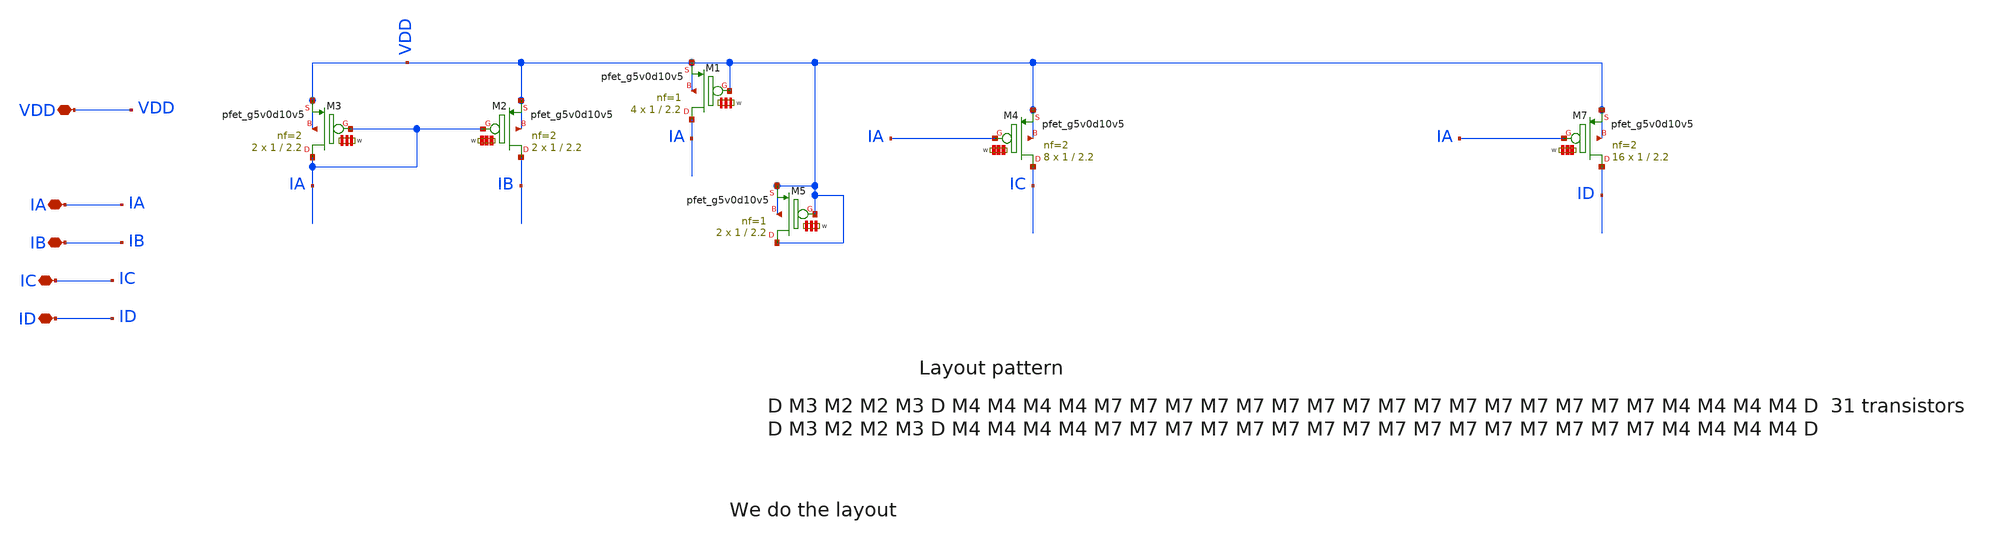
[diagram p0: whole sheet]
** sch_path: Learning/single_ended_amplifiers/Design_and_Analysis_of_Two-Stage_CMOS_Operational_Amplifier_for_Fluorescence_Signal_Processing_sky130_5V/klayout_layout/Pmos_current_mirror.sch
**.subckt Pmos_current_mirror VDD IA IB IC ID
*.iopin VDD
*.iopin IA
*.iopin IB
*.iopin IC
*.iopin ID
XM2 IB IA VDD VDD sky130_fd_pr__pfet_g5v0d10v5 L=2.2 W='1 * 2 ' nf=2 ad='int((2 + 1)/2) * 1 * 0.29' as='int((2 + 2)/2) * 1 * 0.29'
+ pd='2*int((2 + 1)/2) * (1 + 0.29)' ps='2*int((2 + 2)/2) * (1 + 0.29)' nrd='0.29 / 1 / 2 ' nrs='0.29 / 1 / 2 '
+ sa=0 sb=0 sd=0 mult=2 m=2
XM3 IA IA VDD VDD sky130_fd_pr__pfet_g5v0d10v5 L=2.2 W='1 * 2 ' nf=2 ad='int((2 + 1)/2) * 1 * 0.29' as='int((2 + 2)/2) * 1 * 0.29'
+ pd='2*int((2 + 1)/2) * (1 + 0.29)' ps='2*int((2 + 2)/2) * (1 + 0.29)' nrd='0.29 / 1 / 2 ' nrs='0.29 / 1 / 2 '
+ sa=0 sb=0 sd=0 mult=2 m=2
XM4 IC IA VDD VDD sky130_fd_pr__pfet_g5v0d10v5 L=2.2 W='1 * 2 ' nf=2 ad='int((2 + 1)/2) * 1 * 0.29' as='int((2 + 2)/2) * 1 * 0.29'
+ pd='2*int((2 + 1)/2) * (1 + 0.29)' ps='2*int((2 + 2)/2) * (1 + 0.29)' nrd='0.29 / 1 / 2 ' nrs='0.29 / 1 / 2 '
+ sa=0 sb=0 sd=0 mult=8 m=8
XM7 ID IA VDD VDD sky130_fd_pr__pfet_g5v0d10v5 L=2.2 W='1 * 2 ' nf=2 ad='int((2 + 1)/2) * 1 * 0.29' as='int((2 + 2)/2) * 1 * 0.29'
+ pd='2*int((2 + 1)/2) * (1 + 0.29)' ps='2*int((2 + 2)/2) * (1 + 0.29)' nrd='0.29 / 1 / 2 ' nrs='0.29 / 1 / 2 '
+ sa=0 sb=0 sd=0 mult=16 m=16
XM1 IA VDD VDD VDD sky130_fd_pr__pfet_g5v0d10v5 L=2.2 W='1 * 1 ' nf=1 ad='int((1 + 1)/2) * 1 * 0.29'
+ as='int((1 + 2)/2) * 1 * 0.29' pd='2*int((1 + 1)/2) * (1 + 0.29)' ps='2*int((1 + 2)/2) * (1 + 0.29)'
+ nrd='0.29 / 1 / 1 ' nrs='0.29 / 1 / 1 ' sa=0 sb=0 sd=0 mult=4 m=4
XM5 VDD VDD VDD VDD sky130_fd_pr__pfet_g5v0d10v5 L=2.2 W='1 * 1 ' nf=1 ad='int((1 + 1)/2) * 1 * 0.29'
+ as='int((1 + 2)/2) * 1 * 0.29' pd='2*int((1 + 1)/2) * (1 + 0.29)' ps='2*int((1 + 2)/2) * (1 + 0.29)'
+ nrd='0.29 / 1 / 1 ' nrs='0.29 / 1 / 1 ' sa=0 sb=0 sd=0 mult=2 m=2
**.ends
.end
